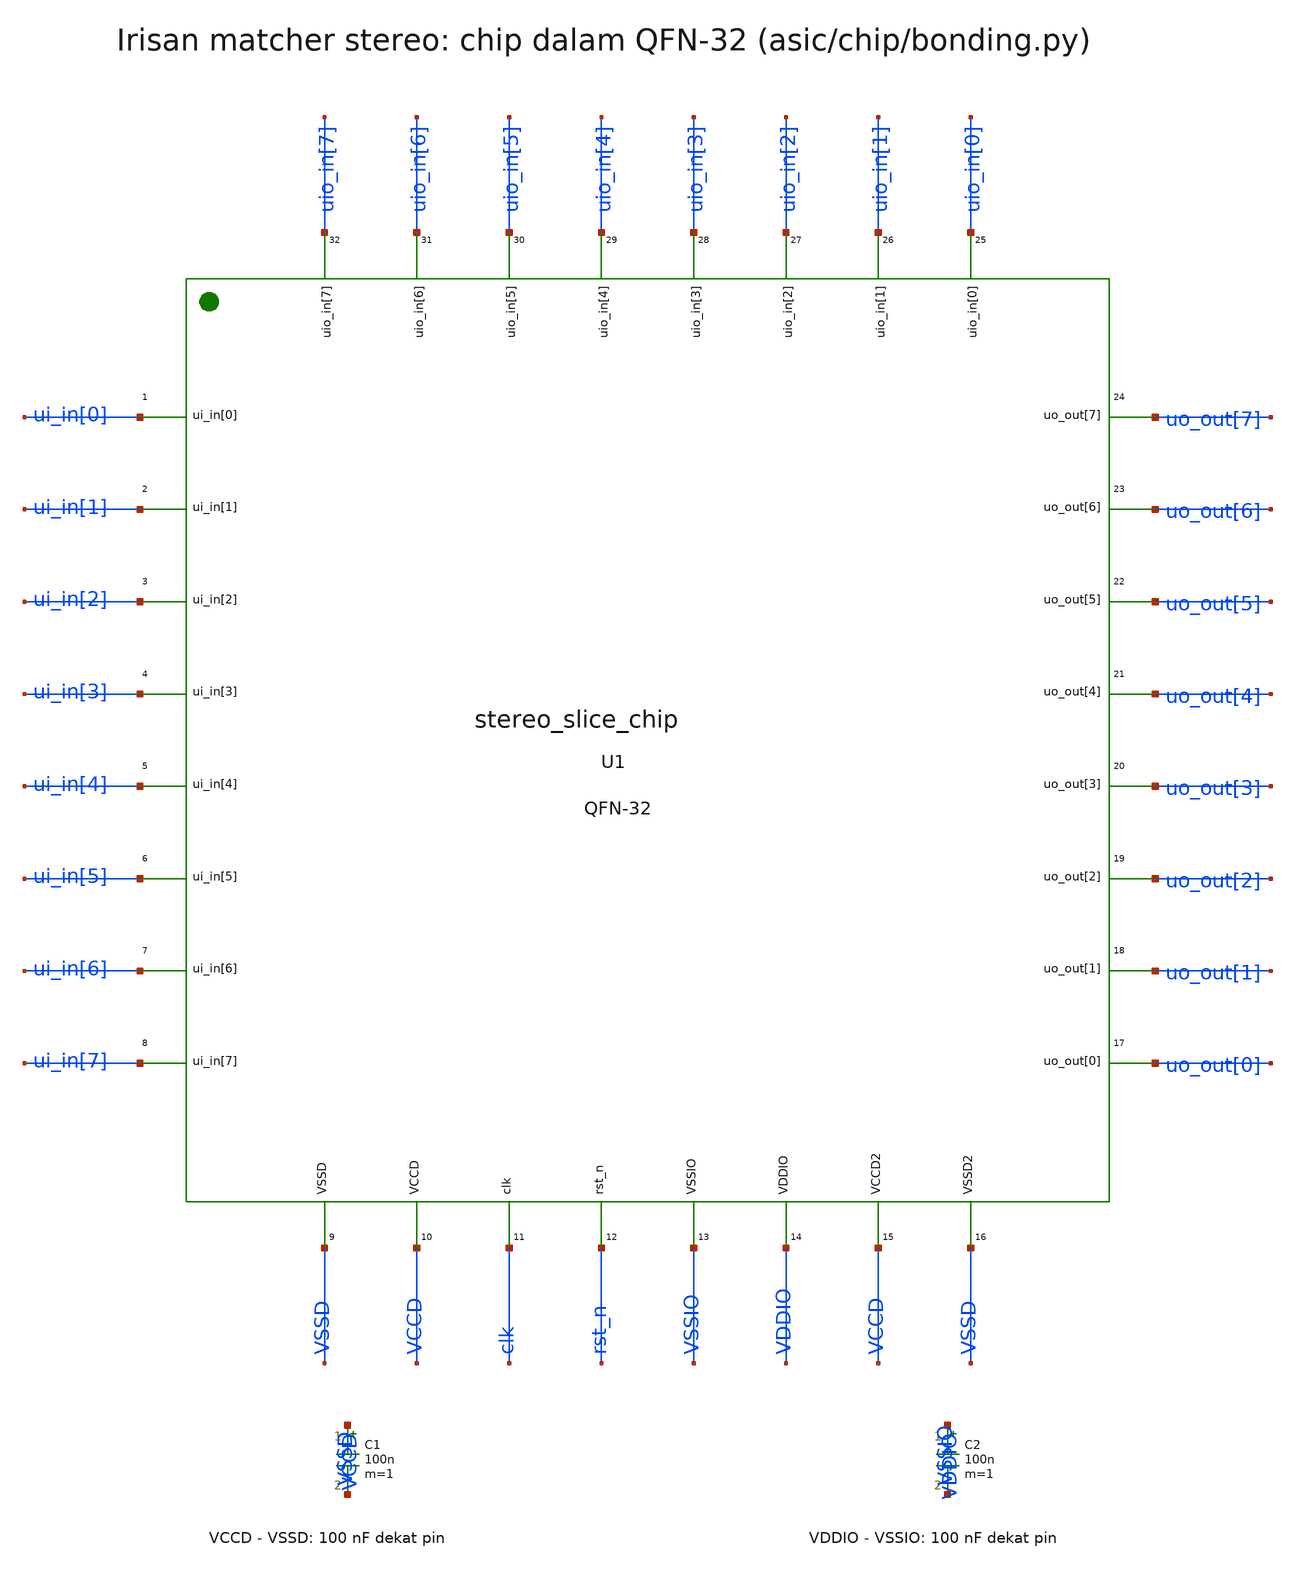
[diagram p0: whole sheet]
** sch_path: asic/chip/out/xschem/stereo_slice_chip_tb.sch
**.subckt stereo_slice_chip_tb
U1 ui_in[0] ui_in[1] ui_in[2] ui_in[3] ui_in[4] ui_in[5] ui_in[6] ui_in[7] VSSD VCCD clk rst_n VSSIO
+ VDDIO VCCD VSSD uo_out[0] uo_out[1] uo_out[2] uo_out[3] uo_out[4] uo_out[5] uo_out[6] uo_out[7] uio_in[0]
+ uio_in[1] uio_in[2] uio_in[3] uio_in[4] uio_in[5] uio_in[6] uio_in[7] stereo_slice_chip
C1 VCCD VSSD 100n m=1
C2 VDDIO VSSIO 100n m=1
**.ends
.end
